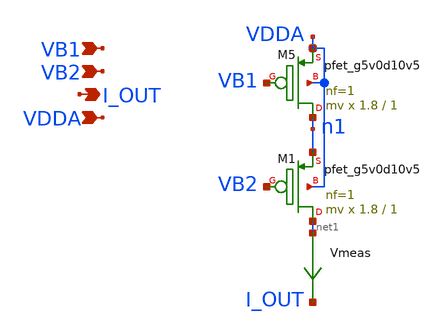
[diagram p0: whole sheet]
** sch_path: xschem/head.sch
**.subckt head I_OUT VB1 VB2 VDDA
*.opin I_OUT
*.ipin VB1
*.ipin VB2
*.ipin VDDA
XM5 n1 VB1 VDDA VDDA sky130_fd_pr__pfet_g5v0d10v5 L=1 W=1.8 nf=1 ad='int((nf+1)/2) * W/nf * 0.29' as='int((nf+2)/2) * W/nf * 0.29'
+ pd='2*int((nf+1)/2) * (W/nf + 0.29)' ps='2*int((nf+2)/2) * (W/nf + 0.29)' nrd='0.29 / W' nrs='0.29 / W'
+ sa=0 sb=0 sd=0 mult=mv m=mv
XM1 net1 VB2 n1 VDDA sky130_fd_pr__pfet_g5v0d10v5 L=1 W=1.8 nf=1 ad='int((nf+1)/2) * W/nf * 0.29' as='int((nf+2)/2) * W/nf * 0.29'
+ pd='2*int((nf+1)/2) * (W/nf + 0.29)' ps='2*int((nf+2)/2) * (W/nf + 0.29)' nrd='0.29 / W' nrs='0.29 / W'
+ sa=0 sb=0 sd=0 mult=mv m=mv
Vmeas net1 I_OUT 0
.save i(vmeas)
**.ends
.end
